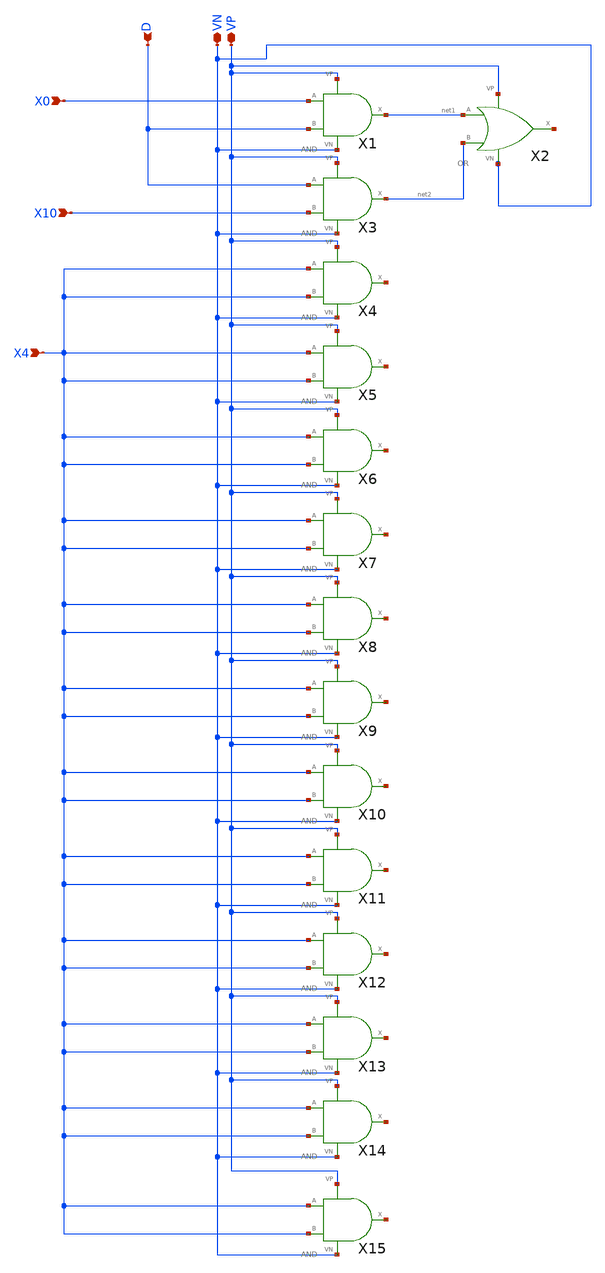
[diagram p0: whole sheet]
** sch_path: projekat_spice/layout/shifter/SHIFTER_debug.sch
**.subckt SHIFTER_debug VP VN X0 X4 X10 D
*.iopin VP
*.iopin VN
*.ipin X0
*.ipin X4
*.ipin X10
*.ipin D
X1 X0 D net1 VP VN AND
X3 D X10 net2 VP VN AND
X4 X4 X4 net3 VP VN AND
X5 X4 X4 net4 VP VN AND
X6 X4 X4 net5 VP VN AND
X7 X4 X4 net6 VP VN AND
X8 X4 X4 net7 VP VN AND
X9 X4 X4 net8 VP VN AND
X10 X4 X4 net9 VP VN AND
X11 X4 X4 net10 VP VN AND
X12 X4 X4 net11 VP VN AND
X13 X4 X4 net12 VP VN AND
X14 X4 X4 net13 VP VN AND
X15 X4 X4 net14 VP VN AND
X2 net1 net2 net15 VP VN OR
**.ends

* expanding   symbol:  /home/mihailo/projekat_sky130/projekat_layout/and/AND.sym # of pins=5
** sym_path: projekat_spice/layout/and/AND.sym
** sch_path: projekat_spice/layout/and/AND.sch
.subckt AND A B X VP VN
*.ipin A
*.ipin B
*.iopin VN
*.iopin VP
*.opin X
XM1 net1 A net2 VN sky130_fd_pr__nfet_01v8 L=0.15 W=1 nf=1 ad='int((nf+1)/2) * W/nf * 0.29' as='int((nf+2)/2) * W/nf * 0.29'
+ pd='2*int((nf+1)/2) * (W/nf + 0.29)' ps='2*int((nf+2)/2) * (W/nf + 0.29)' nrd='0.29 / W' nrs='0.29 / W'
+ sa=0 sb=0 sd=0 mult=1 m=1
XM2 net1 A VP VP sky130_fd_pr__pfet_01v8 L=0.15 W=1 nf=1 ad='int((nf+1)/2) * W/nf * 0.29' as='int((nf+2)/2) * W/nf * 0.29'
+ pd='2*int((nf+1)/2) * (W/nf + 0.29)' ps='2*int((nf+2)/2) * (W/nf + 0.29)' nrd='0.29 / W' nrs='0.29 / W'
+ sa=0 sb=0 sd=0 mult=1 m=1
XM3 net1 B VP VP sky130_fd_pr__pfet_01v8 L=0.15 W=1 nf=1 ad='int((nf+1)/2) * W/nf * 0.29' as='int((nf+2)/2) * W/nf * 0.29'
+ pd='2*int((nf+1)/2) * (W/nf + 0.29)' ps='2*int((nf+2)/2) * (W/nf + 0.29)' nrd='0.29 / W' nrs='0.29 / W'
+ sa=0 sb=0 sd=0 mult=1 m=1
XM4 net2 B VN VN sky130_fd_pr__nfet_01v8 L=0.15 W=1 nf=1 ad='int((nf+1)/2) * W/nf * 0.29' as='int((nf+2)/2) * W/nf * 0.29'
+ pd='2*int((nf+1)/2) * (W/nf + 0.29)' ps='2*int((nf+2)/2) * (W/nf + 0.29)' nrd='0.29 / W' nrs='0.29 / W'
+ sa=0 sb=0 sd=0 mult=1 m=1
XM5 X net1 VN VN sky130_fd_pr__nfet_01v8 L=0.15 W=1 nf=1 ad='int((nf+1)/2) * W/nf * 0.29' as='int((nf+2)/2) * W/nf * 0.29'
+ pd='2*int((nf+1)/2) * (W/nf + 0.29)' ps='2*int((nf+2)/2) * (W/nf + 0.29)' nrd='0.29 / W' nrs='0.29 / W'
+ sa=0 sb=0 sd=0 mult=1 m=1
XM6 X net1 VP VP sky130_fd_pr__pfet_01v8 L=0.15 W=1 nf=1 ad='int((nf+1)/2) * W/nf * 0.29' as='int((nf+2)/2) * W/nf * 0.29'
+ pd='2*int((nf+1)/2) * (W/nf + 0.29)' ps='2*int((nf+2)/2) * (W/nf + 0.29)' nrd='0.29 / W' nrs='0.29 / W'
+ sa=0 sb=0 sd=0 mult=1 m=1
.ends


* expanding   symbol:  /home/mihailo/projekat_sky130/projekat_layout/or/OR.sym # of pins=5
** sym_path: projekat_spice/layout/or/OR.sym
** sch_path: projekat_spice/layout/or/OR.sch
.subckt OR A B X VP VN
*.opin X
*.ipin A
*.ipin B
*.iopin VP
*.iopin VN
XM1 net2 A VN VN sky130_fd_pr__nfet_01v8 L=0.15 W=1 nf=1 ad='int((nf+1)/2) * W/nf * 0.29' as='int((nf+2)/2) * W/nf * 0.29'
+ pd='2*int((nf+1)/2) * (W/nf + 0.29)' ps='2*int((nf+2)/2) * (W/nf + 0.29)' nrd='0.29 / W' nrs='0.29 / W'
+ sa=0 sb=0 sd=0 mult=1 m=1
XM2 net1 A VP VP sky130_fd_pr__pfet_01v8 L=0.15 W=1 nf=1 ad='int((nf+1)/2) * W/nf * 0.29' as='int((nf+2)/2) * W/nf * 0.29'
+ pd='2*int((nf+1)/2) * (W/nf + 0.29)' ps='2*int((nf+2)/2) * (W/nf + 0.29)' nrd='0.29 / W' nrs='0.29 / W'
+ sa=0 sb=0 sd=0 mult=1 m=1
XM3 net2 B net1 VP sky130_fd_pr__pfet_01v8 L=0.15 W=1 nf=1 ad='int((nf+1)/2) * W/nf * 0.29' as='int((nf+2)/2) * W/nf * 0.29'
+ pd='2*int((nf+1)/2) * (W/nf + 0.29)' ps='2*int((nf+2)/2) * (W/nf + 0.29)' nrd='0.29 / W' nrs='0.29 / W'
+ sa=0 sb=0 sd=0 mult=1 m=1
XM4 net2 B VN VN sky130_fd_pr__nfet_01v8 L=0.15 W=1 nf=1 ad='int((nf+1)/2) * W/nf * 0.29' as='int((nf+2)/2) * W/nf * 0.29'
+ pd='2*int((nf+1)/2) * (W/nf + 0.29)' ps='2*int((nf+2)/2) * (W/nf + 0.29)' nrd='0.29 / W' nrs='0.29 / W'
+ sa=0 sb=0 sd=0 mult=1 m=1
XM5 X net2 VN VN sky130_fd_pr__nfet_01v8 L=0.15 W=1 nf=1 ad='int((nf+1)/2) * W/nf * 0.29' as='int((nf+2)/2) * W/nf * 0.29'
+ pd='2*int((nf+1)/2) * (W/nf + 0.29)' ps='2*int((nf+2)/2) * (W/nf + 0.29)' nrd='0.29 / W' nrs='0.29 / W'
+ sa=0 sb=0 sd=0 mult=1 m=1
XM6 X net2 VP VP sky130_fd_pr__pfet_01v8 L=0.15 W=1 nf=1 ad='int((nf+1)/2) * W/nf * 0.29' as='int((nf+2)/2) * W/nf * 0.29'
+ pd='2*int((nf+1)/2) * (W/nf + 0.29)' ps='2*int((nf+2)/2) * (W/nf + 0.29)' nrd='0.29 / W' nrs='0.29 / W'
+ sa=0 sb=0 sd=0 mult=1 m=1
.ends

.end
